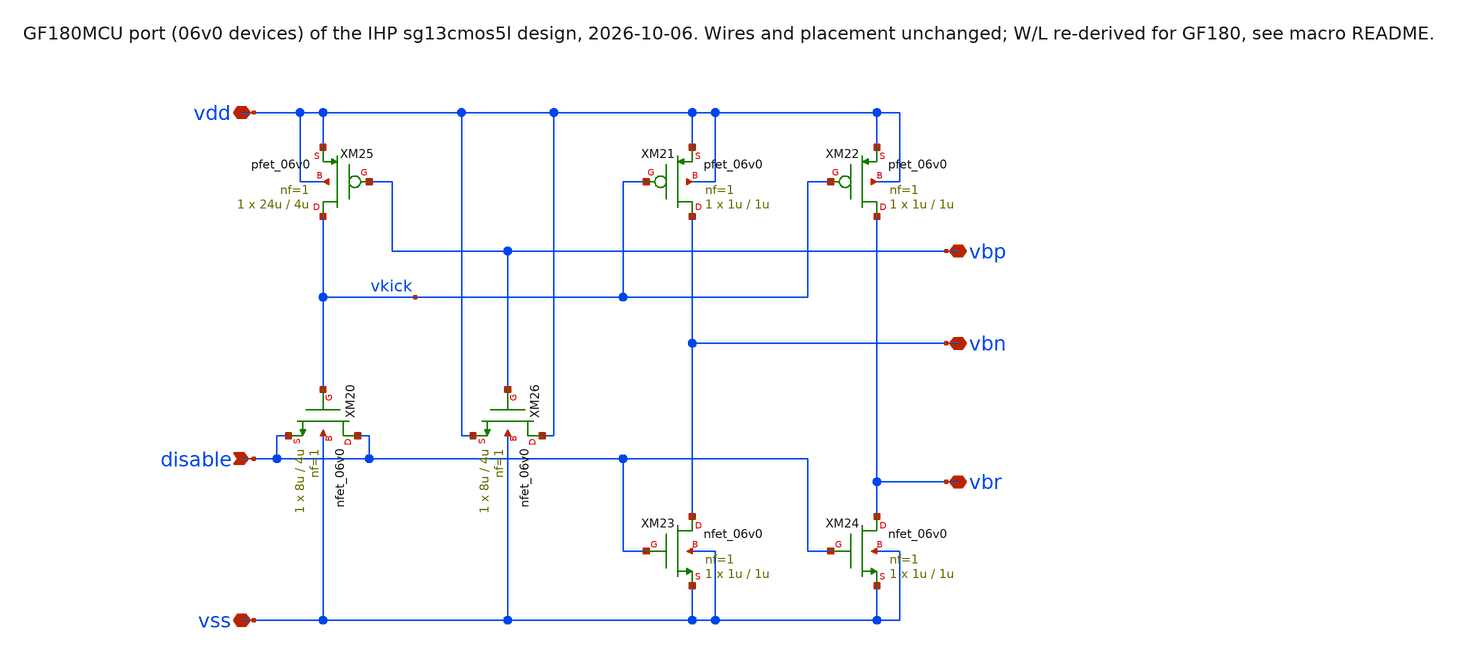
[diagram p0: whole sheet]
** sch_path: macros/OgueyAebischerBias/schematic/xschem/ToBiasStartup_06v0.sch
**.subckt ToBiasStartup_06v0 vss vdd vbp vbn vbr disable
*.iopin vss
*.iopin vdd
*.iopin vbp
*.iopin vbn
*.iopin vbr
*.ipin disable
XM24 vbr disable vss vss nfet_06v0 L=1u W=1u nf=1 ad='int((nf+1)/2) * W/nf * 0.18u' as='int((nf+2)/2) * W/nf * 0.18u'
+ pd='2*int((nf+1)/2) * (W/nf + 0.18u)' ps='2*int((nf+2)/2) * (W/nf + 0.18u)' nrd='0.18u / W' nrs='0.18u / W'
+ sa=0 sb=0 sd=0 m=1
XM22 vbr vkick vdd vdd pfet_06v0 L=1u W=1u nf=1 ad='int((nf+1)/2) * W/nf * 0.18u' as='int((nf+2)/2) * W/nf * 0.18u'
+ pd='2*int((nf+1)/2) * (W/nf + 0.18u)' ps='2*int((nf+2)/2) * (W/nf + 0.18u)' nrd='0.18u / W' nrs='0.18u / W'
+ sa=0 sb=0 sd=0 m=1
XM25 vkick vbp vdd vdd pfet_06v0 L=4u W=24u nf=1 ad='int((nf+1)/2) * W/nf * 0.18u' as='int((nf+2)/2) * W/nf * 0.18u'
+ pd='2*int((nf+1)/2) * (W/nf + 0.18u)' ps='2*int((nf+2)/2) * (W/nf + 0.18u)' nrd='0.18u / W' nrs='0.18u / W'
+ sa=0 sb=0 sd=0 m=1
XM23 vbn disable vss vss nfet_06v0 L=1u W=1u nf=1 ad='int((nf+1)/2) * W/nf * 0.18u' as='int((nf+2)/2) * W/nf * 0.18u'
+ pd='2*int((nf+1)/2) * (W/nf + 0.18u)' ps='2*int((nf+2)/2) * (W/nf + 0.18u)' nrd='0.18u / W' nrs='0.18u / W'
+ sa=0 sb=0 sd=0 m=1
XM21 vbn vkick vdd vdd pfet_06v0 L=1u W=1u nf=1 ad='int((nf+1)/2) * W/nf * 0.18u' as='int((nf+2)/2) * W/nf * 0.18u'
+ pd='2*int((nf+1)/2) * (W/nf + 0.18u)' ps='2*int((nf+2)/2) * (W/nf + 0.18u)' nrd='0.18u / W' nrs='0.18u / W'
+ sa=0 sb=0 sd=0 m=1
XM20 disable vkick disable vss nfet_06v0 L=4u W=8u nf=1 ad='int((nf+1)/2) * W/nf * 0.18u' as='int((nf+2)/2) * W/nf * 0.18u'
+ pd='2*int((nf+1)/2) * (W/nf + 0.18u)' ps='2*int((nf+2)/2) * (W/nf + 0.18u)' nrd='0.18u / W' nrs='0.18u / W'
+ sa=0 sb=0 sd=0 m=1
XM26 vdd vbp vdd vss nfet_06v0 L=4u W=8u nf=1 ad='int((nf+1)/2) * W/nf * 0.18u' as='int((nf+2)/2) * W/nf * 0.18u'
+ pd='2*int((nf+1)/2) * (W/nf + 0.18u)' ps='2*int((nf+2)/2) * (W/nf + 0.18u)' nrd='0.18u / W' nrs='0.18u / W'
+ sa=0 sb=0 sd=0 m=1
**.ends
.end
